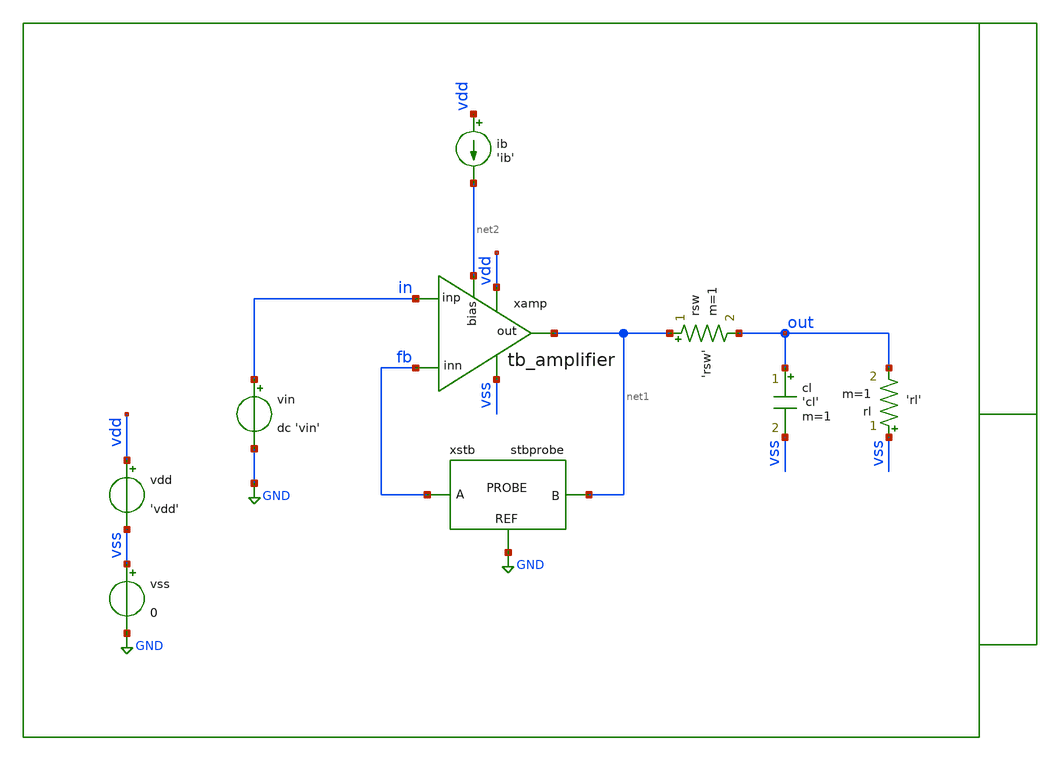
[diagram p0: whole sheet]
** sch_path: xschem/tb/testbuffer/tb_amplifier/ac_tb_amplifier_stb.sch
**.subckt ac_tb_amplifier_stb
vin in GND dc 'vin'
cl out vss 'cl' m=1
ib vdd net2 'ib'
rl vss out 'rl' m=1
vdd vdd vss 'vdd'
vss vss GND 0
xamp vdd net1 in fb vss net2 tb_amplifier
rsw net1 out 'rsw' m=1
xstb fb net1 GND stbprobe
**** begin user architecture code

* Control

.param vdd=3.3
.param vcm='vdd/2'
.param vin='vcm'
.param ib=5u
.param cl=10p
.param rl=1e6
.param rsw=1

.control

let runs=2
let run=0

alter v.xstb.vprobe1 acmag=1
alter i.xstb.iprobe1 acmag=0

dowhile run < runs
set run ="$&run"

ac dec 100 0.01 10G

alter v.xstb.vprobe1 acmag=0
alter i.xstb.iprobe1 acmag=1

let run = run + 1

end

let ip11 = ac1.i(v.xstb.vprobe1)
let ip12 = ac1.i(v.xstb.vprobe2)
let ip21 = ac2.i(v.xstb.vprobe1)
let ip22 = ac2.i(v.xstb.vprobe2)
let vprb1 = ac1.v(xstb.probe)
let vprb2 = ac2.v(xstb.probe)

let av = 1/(1/(2*(ip11*vprb2-vprb1*ip21)+vprb1+ip21)-1)

let phase=180/PI*cph(av)

gnuplot p1 vdb(av)
gnuplot p2 phase

meas ac gain find vdb(av) at=0.01
meas ac ugbw when vdb(av)=0
meas ac pm_pha find phase when vdb(av)=0

let pm = 180 + pm_pha
print gain
print ugbw
print pm

set wr_singlescale
set wr_vecnames
wrdata data.csv vdb(av) phase

.endc


 * Model Corners

.include $::CORNERS/ngspice/tt.spice
*.include $::CORNERS/ngspice/ff.spice
*.include $::CORNERS/ngspice/ss.spice
*.include $::CORNERS/ngspice/sf.spice
*.include $::CORNERS/ngspice/fs.spice

**** end user architecture code
**.ends

* expanding   symbol:  sch/testbuffer/tb_amplifier/tb_amplifier.sym # of pins=6
** sym_path: xschem/sch/testbuffer/tb_amplifier/tb_amplifier.sym
** sch_path: xschem/sch/testbuffer/tb_amplifier/tb_amplifier.sch
.subckt tb_amplifier vdd out inp inn vss bias
*.ipin inn
*.ipin inp
*.opin out
*.iopin bias
*.iopin vdd
*.iopin vss
XM3 mirr mirr vdd vdd pfet_06v0 L=4u W=16u nf=2 ad='int((nf+1)/2) * W/nf * 0.18u' as='int((nf+2)/2) * W/nf * 0.18u'
+ pd='2*int((nf+1)/2) * (W/nf + 0.18u)' ps='2*int((nf+2)/2) * (W/nf + 0.18u)' nrd='0.18u / W' nrs='0.18u / W'
+ sa=0 sb=0 sd=0 m=2 par=2
XM4 comp mirr vdd vdd pfet_06v0 L=4u W=16u nf=2 ad='int((nf+1)/2) * W/nf * 0.18u' as='int((nf+2)/2) * W/nf * 0.18u'
+ pd='2*int((nf+1)/2) * (W/nf + 0.18u)' ps='2*int((nf+2)/2) * (W/nf + 0.18u)' nrd='0.18u / W' nrs='0.18u / W'
+ sa=0 sb=0 sd=0 m=2 par=2
XM2 comp inp vcm vss nfet_06v0 L=2u W=16u nf=2 ad='int((nf+1)/2) * W/nf * 0.18u' as='int((nf+2)/2) * W/nf * 0.18u'
+ pd='2*int((nf+1)/2) * (W/nf + 0.18u)' ps='2*int((nf+2)/2) * (W/nf + 0.18u)' nrd='0.18u / W' nrs='0.18u / W'
+ sa=0 sb=0 sd=0 m=2 par=2
XM1 mirr inn vcm vss nfet_06v0 L=2u W=16u nf=2 ad='int((nf+1)/2) * W/nf * 0.18u' as='int((nf+2)/2) * W/nf * 0.18u'
+ pd='2*int((nf+1)/2) * (W/nf + 0.18u)' ps='2*int((nf+2)/2) * (W/nf + 0.18u)' nrd='0.18u / W' nrs='0.18u / W'
+ sa=0 sb=0 sd=0 m=2 par=2
XM5 vcm bias vss vss nfet_06v0 L=1u W=16u nf=2 ad='int((nf+1)/2) * W/nf * 0.18u' as='int((nf+2)/2) * W/nf * 0.18u'
+ pd='2*int((nf+1)/2) * (W/nf + 0.18u)' ps='2*int((nf+2)/2) * (W/nf + 0.18u)' nrd='0.18u / W' nrs='0.18u / W'
+ sa=0 sb=0 sd=0 m=2 par=2
XM6 out bias vss vss nfet_06v0 L=1u W=16u nf=2 ad='int((nf+1)/2) * W/nf * 0.18u' as='int((nf+2)/2) * W/nf * 0.18u'
+ pd='2*int((nf+1)/2) * (W/nf + 0.18u)' ps='2*int((nf+2)/2) * (W/nf + 0.18u)' nrd='0.18u / W' nrs='0.18u / W'
+ sa=0 sb=0 sd=0 m=12 par=12
XM7 out comp vdd vdd pfet_06v0 L=1u W=96u nf=12 ad='int((nf+1)/2) * W/nf * 0.18u' as='int((nf+2)/2) * W/nf * 0.18u'
+ pd='2*int((nf+1)/2) * (W/nf + 0.18u)' ps='2*int((nf+2)/2) * (W/nf + 0.18u)' nrd='0.18u / W' nrs='0.18u / W'
+ sa=0 sb=0 sd=0 m=1 par=1
XMB1 bias bias vss vss nfet_06v0 L=1u W=16u nf=2 ad='int((nf+1)/2) * W/nf * 0.18u' as='int((nf+2)/2) * W/nf * 0.18u'
+ pd='2*int((nf+1)/2) * (W/nf + 0.18u)' ps='2*int((nf+2)/2) * (W/nf + 0.18u)' nrd='0.18u / W' nrs='0.18u / W'
+ sa=0 sb=0 sd=0 m=2 par=2
XMB2 vbm bias vss vss nfet_06v0 L=1u W=16u nf=2 ad='int((nf+1)/2) * W/nf * 0.18u' as='int((nf+2)/2) * W/nf * 0.18u'
+ pd='2*int((nf+1)/2) * (W/nf + 0.18u)' ps='2*int((nf+2)/2) * (W/nf + 0.18u)' nrd='0.18u / W' nrs='0.18u / W'
+ sa=0 sb=0 sd=0 m=2 par=2
XMB3 vbm vbm vbt vdd pfet_06v0 L=1u W=16u nf=2 ad='int((nf+1)/2) * W/nf * 0.18u' as='int((nf+2)/2) * W/nf * 0.18u'
+ pd='2*int((nf+1)/2) * (W/nf + 0.18u)' ps='2*int((nf+2)/2) * (W/nf + 0.18u)' nrd='0.18u / W' nrs='0.18u / W'
+ sa=0 sb=0 sd=0 m=1 par=1
XMB4 vbt vbt vdd vdd pfet_06v0 L=1u W=16u nf=2 ad='int((nf+1)/2) * W/nf * 0.18u' as='int((nf+2)/2) * W/nf * 0.18u'
+ pd='2*int((nf+1)/2) * (W/nf + 0.18u)' ps='2*int((nf+2)/2) * (W/nf + 0.18u)' nrd='0.18u / W' nrs='0.18u / W'
+ sa=0 sb=0 sd=0 m=1 par=1
XRCC gc comp vdd ppolyf_u_1k_6p0 r_width=2e-6 r_length=38e-6 s=1 m=1
XMDUM1 vss vss vss vss nfet_06v0 L=2u W=16u nf=2 ad='int((nf+1)/2) * W/nf * 0.18u' as='int((nf+2)/2) * W/nf * 0.18u'
+ pd='2*int((nf+1)/2) * (W/nf + 0.18u)' ps='2*int((nf+2)/2) * (W/nf + 0.18u)' nrd='0.18u / W' nrs='0.18u / W'
+ sa=0 sb=0 sd=0 m=2 par=2
XMDUM2 vdd vdd vdd vdd pfet_06v0 L=4u W=16u nf=2 ad='int((nf+1)/2) * W/nf * 0.18u' as='int((nf+2)/2) * W/nf * 0.18u'
+ pd='2*int((nf+1)/2) * (W/nf + 0.18u)' ps='2*int((nf+2)/2) * (W/nf + 0.18u)' nrd='0.18u / W' nrs='0.18u / W'
+ sa=0 sb=0 sd=0 m=4 par=4
XC1 out gc cap_mim_2f0_m4m5_noshield c_width=30e-6 c_length=30e-6 m=1
.ends


* expanding   symbol:  xschem/ideal/stbprobe/stbprobe.sym # of pins=3
** sym_path: xschem/xschem/ideal/stbprobe/stbprobe.sym
** sch_path: xschem/xschem/ideal/stbprobe/stbprobe.sch
.subckt stbprobe A B REF
*.iopin A
*.iopin B
*.iopin REF
Vprobe1 probe A 0
Iprobe1 REF probe 0
Vprobe2 probe B 0
**** begin user architecture code



**** end user architecture code
.ends

.GLOBAL GND
.end
